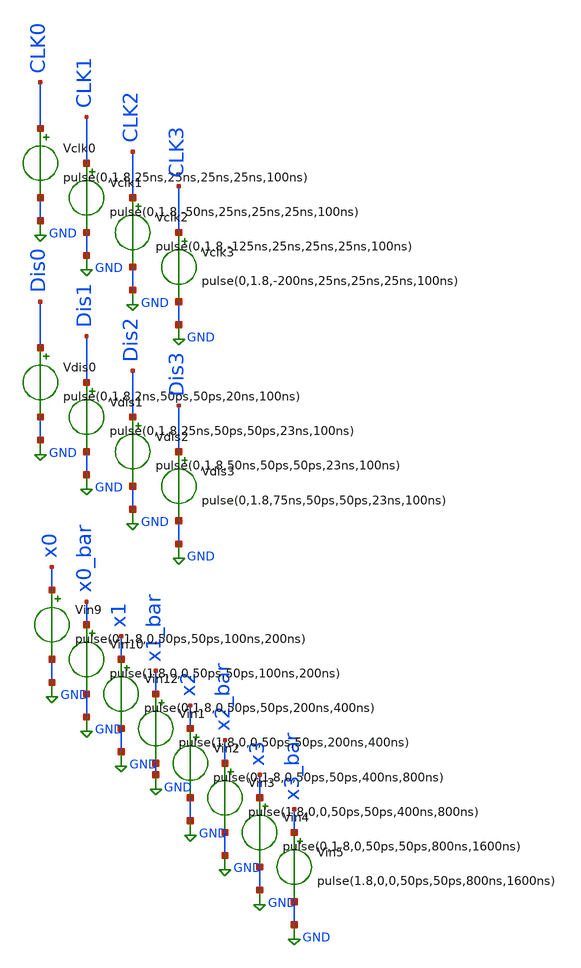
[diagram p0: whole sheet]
** sch_path: skywater_stuff/untitled-11.sch
**.subckt untitled-11
Vin9 x0 GND pulse(0,1.8,0,50ps,50ps,100ns,200ns)
Vin10 x0_bar GND pulse(1.8,0,0,50ps,50ps,100ns,200ns)
Vin12 x1 GND pulse(0,1.8,0,50ps,50ps,200ns,400ns)
Vin1 x1_bar GND pulse(1.8,0,0,50ps,50ps,200ns,400ns)
Vin2 x2 GND pulse(0,1.8,0,50ps,50ps,400ns,800ns)
Vin3 x2_bar GND pulse(1.8,0,0,50ps,50ps,400ns,800ns)
Vin4 x3 GND pulse(0,1.8,0,50ps,50ps,800ns,1600ns)
Vin5 x3_bar GND pulse(1.8,0,0,50ps,50ps,800ns,1600ns)
Vdis0 Dis0 GND pulse(0,1.8,2ns,50ps,50ps,20ns,100ns)
Vclk0 CLK0 GND pulse(0,1.8,25ns,25ns,25ns,25ns,100ns)
Vdis1 Dis1 GND pulse(0,1.8,25ns,50ps,50ps,23ns,100ns)
Vdis2 Dis2 GND pulse(0,1.8,50ns,50ps,50ps,23ns,100ns)
Vdis3 Dis3 GND pulse(0,1.8,75ns,50ps,50ps,23ns,100ns)
Vclk1 CLK1 GND pulse(0,1.8,-50ns,25ns,25ns,25ns,100ns)
Vclk2 CLK2 GND pulse(0,1.8,-125ns,25ns,25ns,25ns,100ns)
Vclk3 CLK3 GND pulse(0,1.8,-200ns,25ns,25ns,25ns,100ns)
**** begin user architecture code

.lib /research/pdk/open_pdks/share/pdk/sky130A/libs.tech/ngspice/sky130.lib.spice tt
.control
save all
tran 0.1n 1600n
plot v(CLK0) v(Dis0)
plot v(s1)
plot v(s1_bar)
let Pinst_CLK0_CLK2 = (v(CLK0)*i(vclk0))+(v(CLK1)*i(vclk1))+(v(CLK2)*i(vclk2))
**let Pinst_CLK0_CLK2_Dis0_Dis2 =
*+ (v(CLK0)*i(vclk0))+(v(Dis0)*i(Vdis0))+(v(CLK1)*i(vclk1))+(v(Dis1)*i(Vdis1))+(v(CLK2)*i(vclk2))+(v(Dis2)*i(Vdis2))
**plot Pinst_CLK0
plot Pinst_CLK0_CLK2
**plot Pinst_CLK0_CLK2_Dis0_Dis2
wrdata EESPFAL_s1_sim.raw Pinst_CLK0_CLK2
wrdata s1_sim_Pinst_test.csv Pinst_CLK0_CLK2
.endc


**** end user architecture code
**.ends
.GLOBAL GND
.end
